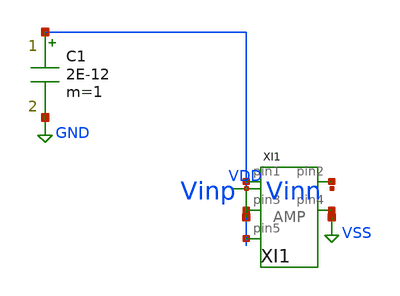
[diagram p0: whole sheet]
** sch_path: data/sch/aicas_AMP_AC_CurrentBias.sch
**.subckt aicas_AMP_AC_CurrentBias
XI1 VDD net1 VDD net2 VDD AMP
C1 VDD GND 2E-12 m=1
**.ends
.GLOBAL VSS
.GLOBAL GND
.GLOBAL VDD
.end
